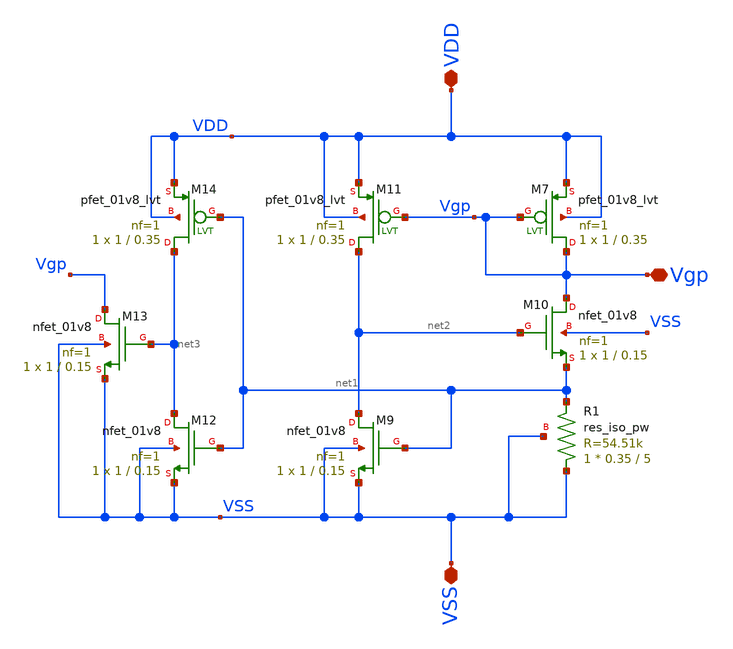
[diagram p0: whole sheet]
** sch_path: xschem/Iref/self_bias.sch
**.subckt self_bias Vgp VDD VSS
*.iopin Vgp
*.iopin VDD
*.iopin VSS
XM9 net2 net1 VSS VSS sky130_fd_pr__nfet_01v8 L=0.15 W=1 nf=1 ad='int((1 + 1)/2) * 1 / 1 * 0.29' as='int((1 + 2)/2) * 1 / 1 * 0.29'
+ pd='2*int((1 + 1)/2) * (1 / 1 + 0.29)' ps='2*int((1 + 2)/2) * (1 / 1 + 0.29)' nrd='0.29 / 1 ' nrs='0.29 / 1 '
+ sa=0 sb=0 sd=0 mult=1 m=1
XM10 Vgp net2 net1 VSS sky130_fd_pr__nfet_01v8 L=0.15 W=1 nf=1 ad='int((1 + 1)/2) * 1 / 1 * 0.29' as='int((1 + 2)/2) * 1 / 1 * 0.29'
+ pd='2*int((1 + 1)/2) * (1 / 1 + 0.29)' ps='2*int((1 + 2)/2) * (1 / 1 + 0.29)' nrd='0.29 / 1 ' nrs='0.29 / 1 '
+ sa=0 sb=0 sd=0 mult=1 m=1
XM12 net3 net1 VSS VSS sky130_fd_pr__nfet_01v8 L=0.15 W=1 nf=1 ad='int((1 + 1)/2) * 1 / 1 * 0.29' as='int((1 + 2)/2) * 1 / 1 * 0.29'
+ pd='2*int((1 + 1)/2) * (1 / 1 + 0.29)' ps='2*int((1 + 2)/2) * (1 / 1 + 0.29)' nrd='0.29 / 1 ' nrs='0.29 / 1 '
+ sa=0 sb=0 sd=0 mult=1 m=1
XM13 Vgp net3 VSS VSS sky130_fd_pr__nfet_01v8 L=0.15 W=1 nf=1 ad='int((1 + 1)/2) * 1 / 1 * 0.29' as='int((1 + 2)/2) * 1 / 1 * 0.29'
+ pd='2*int((1 + 1)/2) * (1 / 1 + 0.29)' ps='2*int((1 + 2)/2) * (1 / 1 + 0.29)' nrd='0.29 / 1 ' nrs='0.29 / 1 '
+ sa=0 sb=0 sd=0 mult=1 m=1
XM7 Vgp Vgp VDD VDD sky130_fd_pr__pfet_01v8_lvt L=0.35 W=1 nf=1 ad='int((1 + 1)/2) * 1 / 1 * 0.29' as='int((1 + 2)/2) * 1 / 1 * 0.29'
+ pd='2*int((1 + 1)/2) * (1 / 1 + 0.29)' ps='2*int((1 + 2)/2) * (1 / 1 + 0.29)' nrd='0.29 / 1 ' nrs='0.29 / 1 '
+ sa=0 sb=0 sd=0 mult=1 m=1
XM11 net2 Vgp VDD VDD sky130_fd_pr__pfet_01v8_lvt L=0.35 W=1 nf=1 ad='int((1 + 1)/2) * 1 / 1 * 0.29'
+ as='int((1 + 2)/2) * 1 / 1 * 0.29' pd='2*int((1 + 1)/2) * (1 / 1 + 0.29)' ps='2*int((1 + 2)/2) * (1 / 1 + 0.29)'
+ nrd='0.29 / 1 ' nrs='0.29 / 1 ' sa=0 sb=0 sd=0 mult=1 m=1
XM14 net3 net1 VDD VDD sky130_fd_pr__pfet_01v8_lvt L=0.35 W=1 nf=1 ad='int((1 + 1)/2) * 1 / 1 * 0.29'
+ as='int((1 + 2)/2) * 1 / 1 * 0.29' pd='2*int((1 + 1)/2) * (1 / 1 + 0.29)' ps='2*int((1 + 2)/2) * (1 / 1 + 0.29)'
+ nrd='0.29 / 1 ' nrs='0.29 / 1 ' sa=0 sb=0 sd=0 mult=1 m=1
XR1 VSS net1 VSS sky130_fd_pr__res_iso_pw W=0.35 L=5 m=1
**.ends
.end
